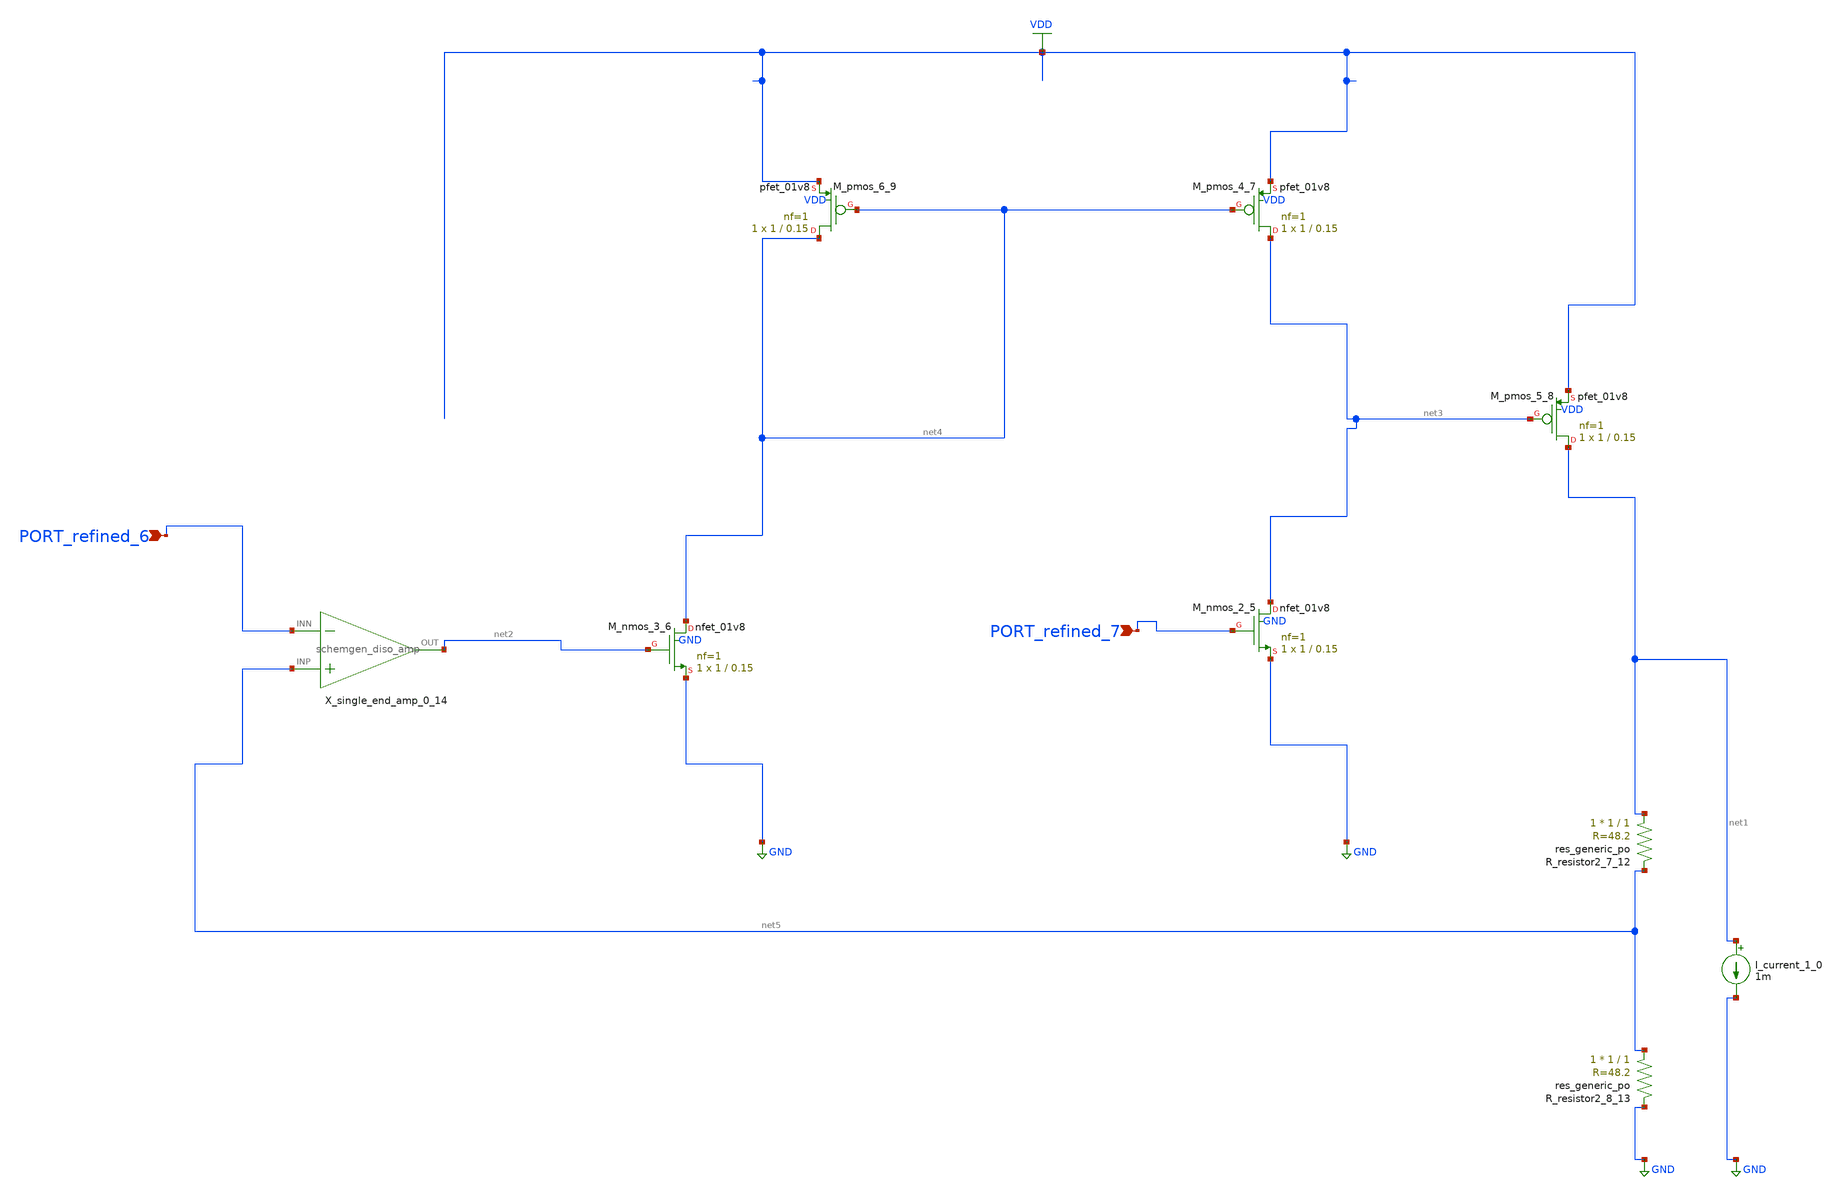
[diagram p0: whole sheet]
** sch_path: schematics/Image2Net/102.sch
**.subckt 102 PORT_refined_6 PORT_refined_7
*.ipin PORT_refined_6
*.ipin PORT_refined_7
I_current_1_0 net1 GND 1m
XM_nmos_2_5 net3 PORT_refined_7 GND GND sky130_fd_pr__nfet_01v8 L=0.15 W=1 nf=1 ad='int((1 + 1)/2) * 1 / 1 * 0.29'
+ as='int((1 + 2)/2) * 1 / 1 * 0.29' pd='2*int((1 + 1)/2) * (1 / 1 + 0.29)' ps='2*int((1 + 2)/2) * (1 / 1 + 0.29)'
+ nrd='0.29 / 1 ' nrs='0.29 / 1 ' sa=0 sb=0 sd=0 mult=1 m=1
XM_nmos_3_6 net4 net2 GND GND sky130_fd_pr__nfet_01v8 L=0.15 W=1 nf=1 ad='int((1 + 1)/2) * 1 / 1 * 0.29'
+ as='int((1 + 2)/2) * 1 / 1 * 0.29' pd='2*int((1 + 1)/2) * (1 / 1 + 0.29)' ps='2*int((1 + 2)/2) * (1 / 1 + 0.29)'
+ nrd='0.29 / 1 ' nrs='0.29 / 1 ' sa=0 sb=0 sd=0 mult=1 m=1
XM_pmos_4_7 net3 net4 VDD VDD sky130_fd_pr__pfet_01v8 L=0.15 W=1 nf=1 ad='int((1 + 1)/2) * 1 / 1 * 0.29'
+ as='int((1 + 2)/2) * 1 / 1 * 0.29' pd='2*int((1 + 1)/2) * (1 / 1 + 0.29)' ps='2*int((1 + 2)/2) * (1 / 1 + 0.29)'
+ nrd='0.29 / 1 ' nrs='0.29 / 1 ' sa=0 sb=0 sd=0 mult=1 m=1
XM_pmos_5_8 net1 net3 VDD VDD sky130_fd_pr__pfet_01v8 L=0.15 W=1 nf=1 ad='int((1 + 1)/2) * 1 / 1 * 0.29'
+ as='int((1 + 2)/2) * 1 / 1 * 0.29' pd='2*int((1 + 1)/2) * (1 / 1 + 0.29)' ps='2*int((1 + 2)/2) * (1 / 1 + 0.29)'
+ nrd='0.29 / 1 ' nrs='0.29 / 1 ' sa=0 sb=0 sd=0 mult=1 m=1
XM_pmos_6_9 net4 net4 VDD VDD sky130_fd_pr__pfet_01v8 L=0.15 W=1 nf=1 ad='int((1 + 1)/2) * 1 / 1 * 0.29'
+ as='int((1 + 2)/2) * 1 / 1 * 0.29' pd='2*int((1 + 1)/2) * (1 / 1 + 0.29)' ps='2*int((1 + 2)/2) * (1 / 1 + 0.29)'
+ nrd='0.29 / 1 ' nrs='0.29 / 1 ' sa=0 sb=0 sd=0 mult=1 m=1
XR_resistor2_7_12 net1 net5 sky130_fd_pr__res_generic_po W=1 L=1 m=1
XR_resistor2_8_13 net5 GND sky130_fd_pr__res_generic_po W=1 L=1 m=1
X_single_end_amp_0_14 net5 PORT_refined_6 net2 schemgen_diso_amp
**.ends

* expanding   symbol:  schemgen_diso_amp.sym # of pins=3
** sym_path: symbols/schemgen_diso_amp.sym
.subckt schemgen_diso_amp INP INN OUT
* SchemGen ideal op-amp: Vout = 1e5 * (V(INP) - V(INN))
E1 OUT 0 INP INN 1e5
.ends schemgen_diso_amp
.GLOBAL GND
.GLOBAL VDD
.end
